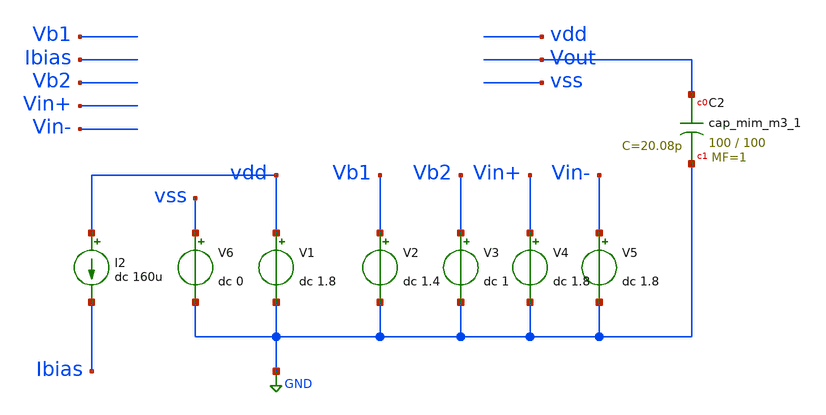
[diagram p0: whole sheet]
** sch_path: tb_fcota_nmos.sch
**.subckt tb_fcota_nmos
I2 vdd Ibias dc 160u
V1 vdd GND dc 1.8
V2 Vb1 GND dc 1.4
V3 Vb2 GND dc 1
V4 Vin+ GND dc 1.8
V5 Vin- GND dc 1.8
V6 vss GND dc 0
XC2 Vout GND sky130_fd_pr__cap_mim_m3_1 W=100 L=100 MF=1 m=1
**.ends
.GLOBAL GND
.end
